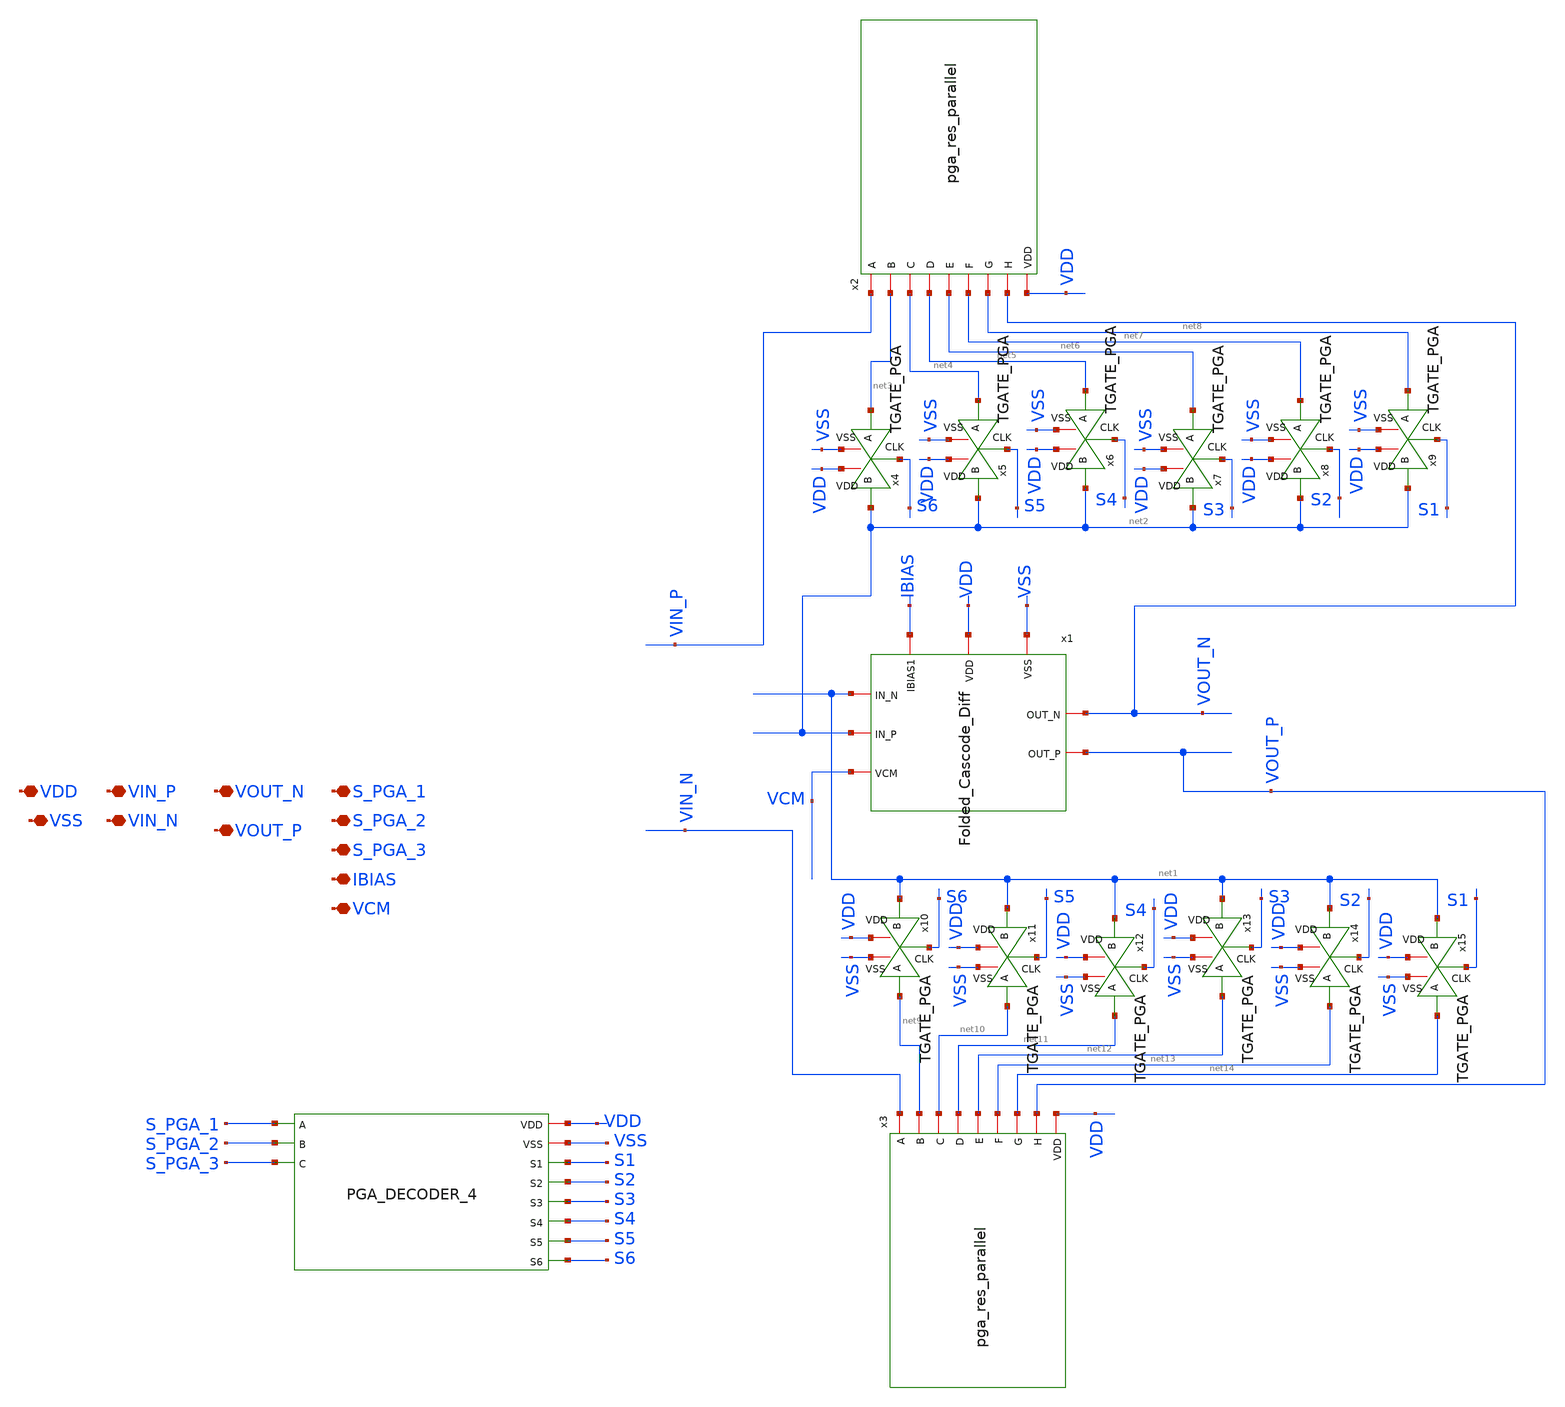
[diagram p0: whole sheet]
** sch_path: AWG_OUTPUT_AND_MUX_PAKISTAN_05/xschem/PGA_FINAL.sch
**.subckt PGA_FINAL VDD VSS VIN_P VOUT_N S_PGA_1 VIN_N VOUT_P S_PGA_2 S_PGA_3 IBIAS VCM
*.iopin VDD
*.iopin VSS
*.iopin VIN_P
*.iopin VOUT_N
*.iopin S_PGA_1
*.iopin VIN_N
*.iopin VOUT_P
*.iopin S_PGA_2
*.iopin S_PGA_3
*.iopin IBIAS
*.iopin VCM
x1 VDD VSS net1 net2 IBIAS VCM VOUT_N VOUT_P Folded_Cascode_Diff
x2 VIN_P net3 net4 net5 net6 net7 net8 VOUT_N VDD pga_res_parallel
x4 VDD net2 S6 net3 VSS TGATE_PGA
x5 VDD net2 S5 net4 VSS TGATE_PGA
x6 VDD net2 S4 net5 VSS TGATE_PGA
x7 VDD net2 S3 net6 VSS TGATE_PGA
x3 VIN_N net9 net10 net11 net12 net13 net14 VOUT_P VDD pga_res_parallel
x10 VDD net1 S6 net9 VSS TGATE_PGA
x11 VDD net1 S5 net10 VSS TGATE_PGA
x12 VDD net1 S4 net11 VSS TGATE_PGA
x13 VDD net1 S3 net12 VSS TGATE_PGA
x16 VDD S6 VSS S4 S3 S5 S2 S1 S_PGA_1 S_PGA_2 S_PGA_3 PGA_DECODER_4
x14 VDD net1 S2 net13 VSS TGATE_PGA
x15 VDD net1 S1 net14 VSS TGATE_PGA
x8 VDD net2 S2 net7 VSS TGATE_PGA
x9 VDD net2 S1 net8 VSS TGATE_PGA
**.ends
.end
